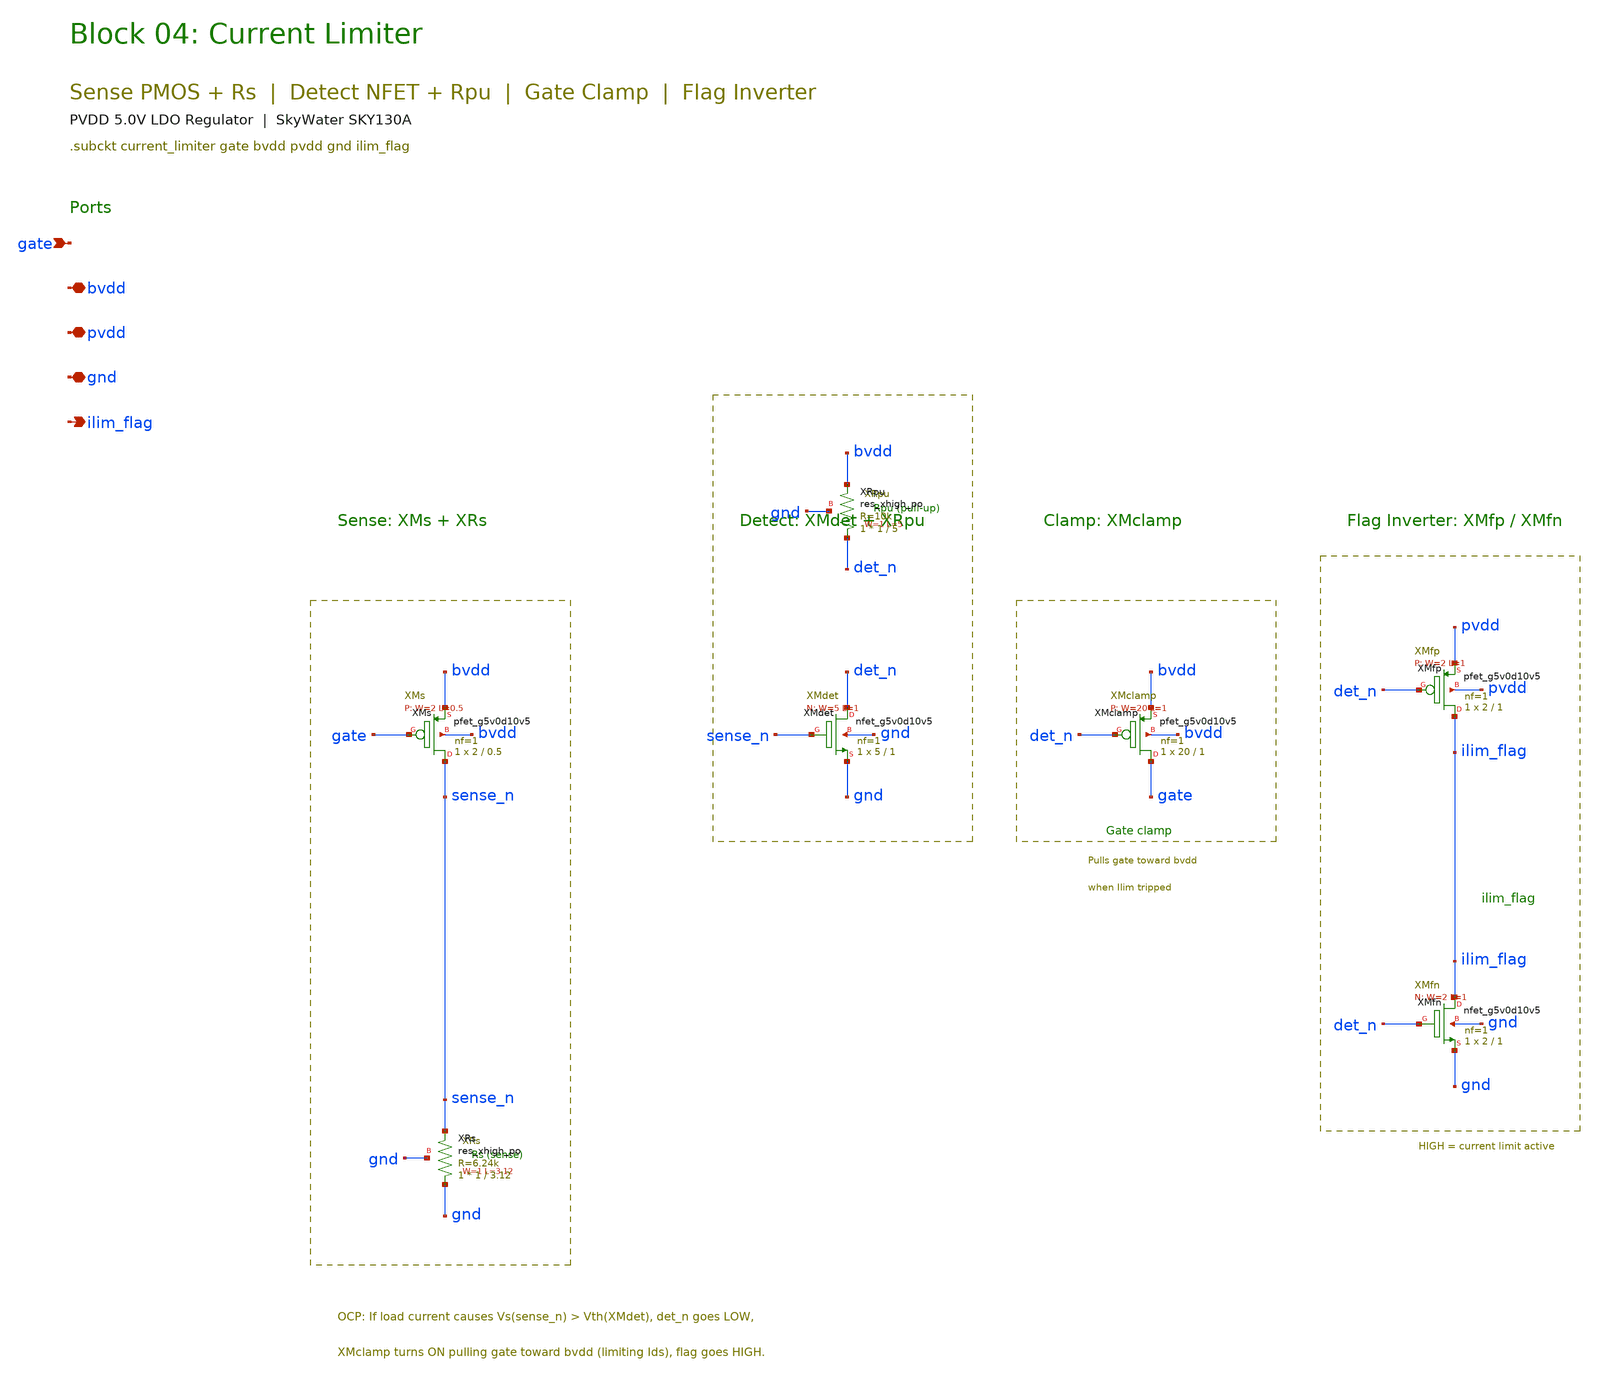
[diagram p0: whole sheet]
** sch_path: pvdd_regulator/10_top_integration/schematics/pvdd_04_current_limiter.sch
**.subckt pvdd_04_current_limiter gate bvdd pvdd gnd ilim_flag
*.ipin gate
*.iopin bvdd
*.iopin pvdd
*.iopin gnd
*.opin ilim_flag
XXMs sense_n gate bvdd bvdd sky130_fd_pr__pfet_g5v0d10v5 L=0.5 W=2 nf=1 ad='int((1 + 1)/2) * 2 / 1 * 0.29'
+ as='int((1 + 2)/2) * 2 / 1 * 0.29' pd='2*int((1 + 1)/2) * (2 / 1 + 0.29)' ps='2*int((1 + 2)/2) * (2 / 1 + 0.29)'
+ nrd='0.29 / 2 ' nrs='0.29 / 2 ' sa=0 sb=0 sd=0 mult=1 m=1
XXRs gnd sense_n gnd sky130_fd_pr__res_xhigh_po W=1 L=3.12 mult=1 m=1
XXMdet det_n sense_n gnd gnd sky130_fd_pr__nfet_g5v0d10v5 L=1 W=5 nf=1 ad='int((1 + 1)/2) * 5 / 1 * 0.29'
+ as='int((1 + 2)/2) * 5 / 1 * 0.29' pd='2*int((1 + 1)/2) * (5 / 1 + 0.29)' ps='2*int((1 + 2)/2) * (5 / 1 + 0.29)'
+ nrd='0.29 / 5 ' nrs='0.29 / 5 ' sa=0 sb=0 sd=0 mult=1 m=1
XXRpu det_n bvdd gnd sky130_fd_pr__res_xhigh_po W=1 L=5 mult=1 m=1
XXMclamp gate det_n bvdd bvdd sky130_fd_pr__pfet_g5v0d10v5 L=1 W=20 nf=1 ad='int((1 + 1)/2) * 20 / 1 * 0.29'
+ as='int((1 + 2)/2) * 20 / 1 * 0.29' pd='2*int((1 + 1)/2) * (20 / 1 + 0.29)' ps='2*int((1 + 2)/2) * (20 / 1 + 0.29)'
+ nrd='0.29 / 20 ' nrs='0.29 / 20 ' sa=0 sb=0 sd=0 mult=1 m=1
XXMfp ilim_flag det_n pvdd pvdd sky130_fd_pr__pfet_g5v0d10v5 L=1 W=2 nf=1 ad='int((1 + 1)/2) * 2 / 1 * 0.29'
+ as='int((1 + 2)/2) * 2 / 1 * 0.29' pd='2*int((1 + 1)/2) * (2 / 1 + 0.29)' ps='2*int((1 + 2)/2) * (2 / 1 + 0.29)'
+ nrd='0.29 / 2 ' nrs='0.29 / 2 ' sa=0 sb=0 sd=0 mult=1 m=1
XXMfn ilim_flag det_n gnd gnd sky130_fd_pr__nfet_g5v0d10v5 L=1 W=2 nf=1 ad='int((1 + 1)/2) * 2 / 1 * 0.29'
+ as='int((1 + 2)/2) * 2 / 1 * 0.29' pd='2*int((1 + 1)/2) * (2 / 1 + 0.29)' ps='2*int((1 + 2)/2) * (2 / 1 + 0.29)'
+ nrd='0.29 / 2 ' nrs='0.29 / 2 ' sa=0 sb=0 sd=0 mult=1 m=1
**.ends
.end
